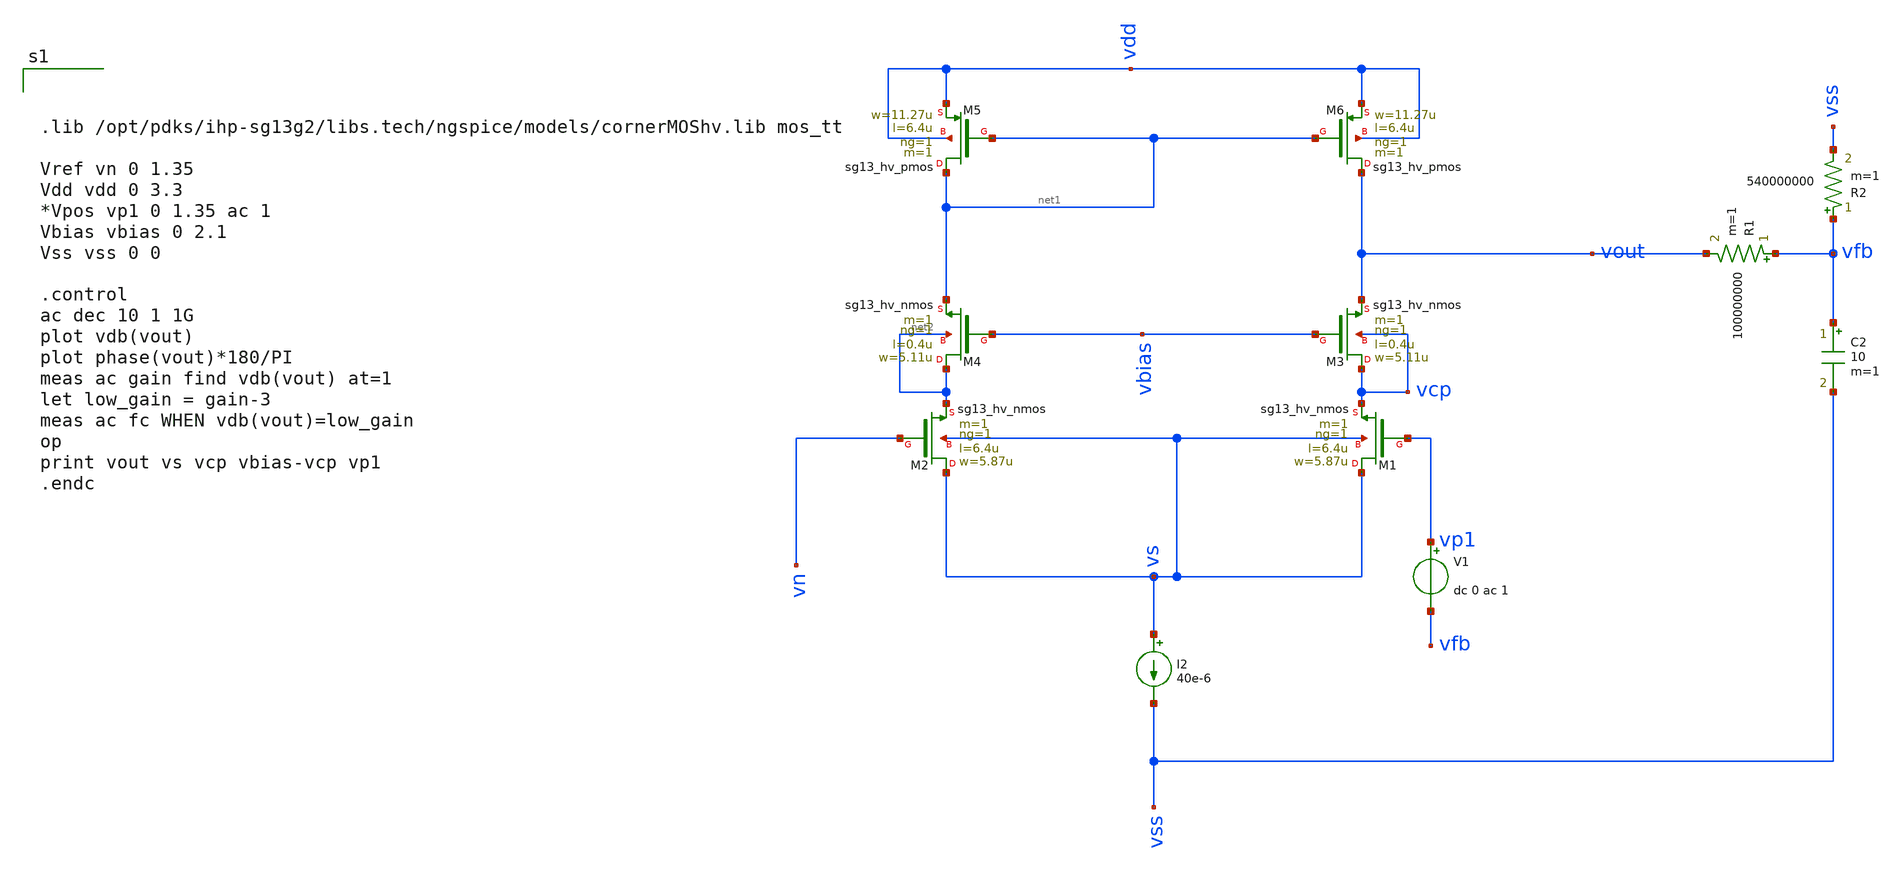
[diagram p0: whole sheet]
** sch_path: test-python/sstadex/xschem/ota_tb_ihp_cc.sch
**.subckt ota_tb_ihp_cc
I2 vs vss 40e-6
XM1 vs vp1 vcp vs sg13_hv_nmos w=5.87u l=6.4u ng=1 m=1 mm_ok=1
XM2 vs vn net2 vs sg13_hv_nmos w=5.87u l=6.4u ng=1 m=1 mm_ok=1
XM3 vcp vbias vout vcp sg13_hv_nmos w=5.11u l=0.4u ng=1 m=1 mm_ok=1
XM4 net2 vbias net1 net2 sg13_hv_nmos w=5.11u l=0.4u ng=1 m=1 mm_ok=1
XM5 net1 net1 vdd vdd sg13_hv_pmos w=11.27u l=6.4u ng=1 m=1 mm_ok=1
XM6 vout net1 vdd vdd sg13_hv_pmos w=11.27u l=6.4u ng=1 m=1 mm_ok=1
R1 vfb vout 100000000 m=1
C2 vfb vss 10 m=1
R2 vfb vss 540000000 m=1
V1 vp1 vfb dc 0 ac 1
**** begin user architecture code



.lib /opt/pdks/ihp-sg13g2/libs.tech/ngspice/models/cornerMOShv.lib mos_tt

Vref vn 0 1.35
Vdd vdd 0 3.3
*Vpos vp1 0 1.35 ac 1
Vbias vbias 0 2.1
Vss vss 0 0

.control
ac dec 10 1 1G
plot vdb(vout)
plot phase(vout)*180/PI
meas ac gain find vdb(vout) at=1
let low_gain = gain-3
meas ac fc WHEN vdb(vout)=low_gain
op
print vout vs vcp vbias-vcp vp1
.endc



**** end user architecture code
**.ends
.end
